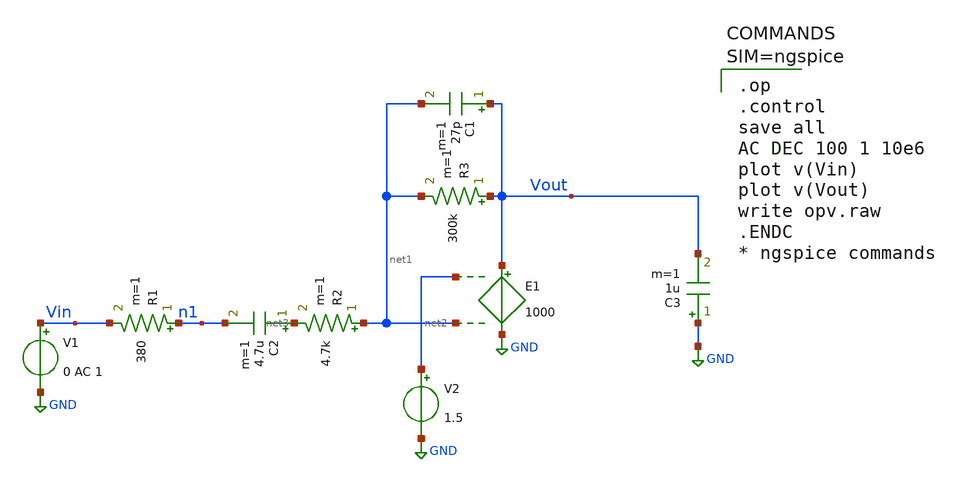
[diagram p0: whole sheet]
** sch_path: xschem/test_1.sch
**.subckt test_1
V1 Vin GND 0 AC 1
R1 n1 Vin 380 m=1
R2 net1 net3 4.7k m=1
C2 net3 n1 4.7u m=1
E1 Vout GND net2 net1 1000
R3 Vout net1 300k m=1
C1 Vout net1 27p m=1
C3 GND Vout 1u m=1
V2 net2 GND 1.5
**** begin user architecture code


.op
.control
save all
AC DEC 100 1 10e6
plot v(Vin)
plot v(Vout)
write opv.raw
.ENDC
* ngspice commands



**** end user architecture code
**.ends
.GLOBAL GND
.end
